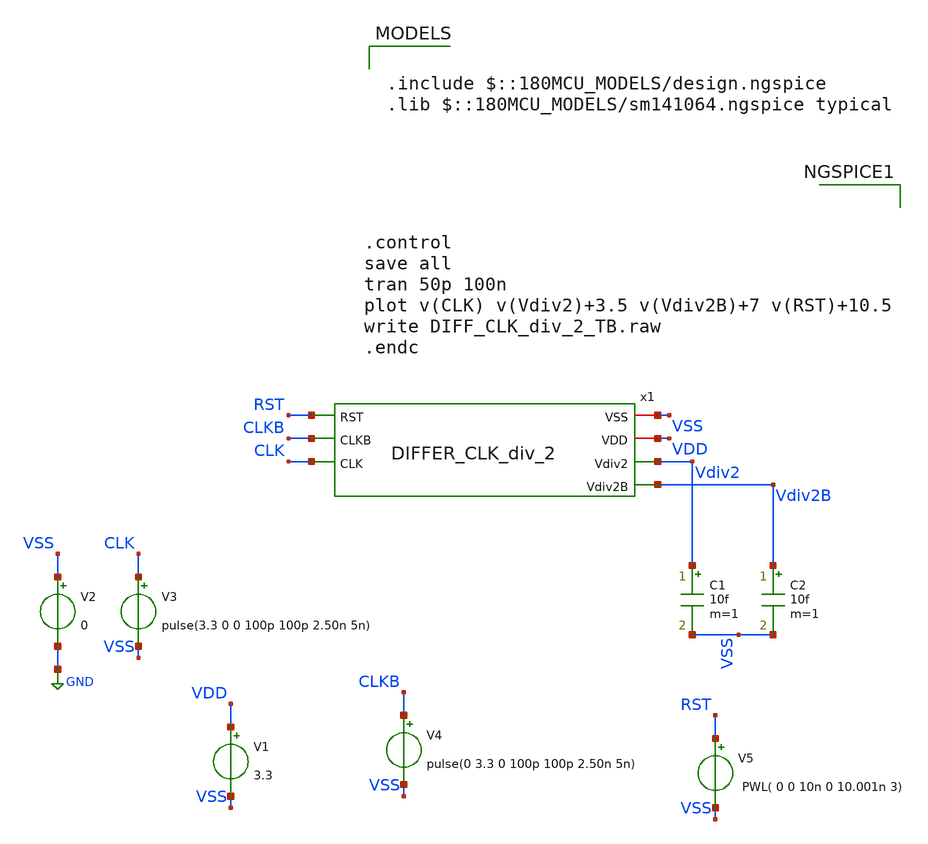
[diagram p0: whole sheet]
** sch_path: Clock_Generator_PAKISTAN_02/xschem/DIFF_CLK_div_2_TB.sch
**.subckt DIFF_CLK_div_2_TB
V1 VDD VSS 3.3
V2 VSS GND 0
V3 CLK VSS pulse(3.3 0 0 100p 100p 2.50n 5n)
C1 Vdiv2 VSS 10f m=1
C2 Vdiv2B VSS 10f m=1
V5 RST VSS PWL( 0 0 10n 0 10.001n 3)
V4 CLKB VSS pulse(0 3.3 0 100p 100p 2.50n 5n)
x1 VSS VDD RST Vdiv2 Vdiv2B CLKB CLK DIFFER_CLK_div_2
**** begin user architecture code

.include $::180MCU_MODELS/design.ngspice
.lib $::180MCU_MODELS/sm141064.ngspice typical




.control
save all
tran 50p 100n
plot v(CLK) v(Vdiv2)+3.5 v(Vdiv2B)+7 v(RST)+10.5
write DIFF_CLK_div_2_TB.raw
.endc


**** end user architecture code
**.ends
.GLOBAL GND
.end
